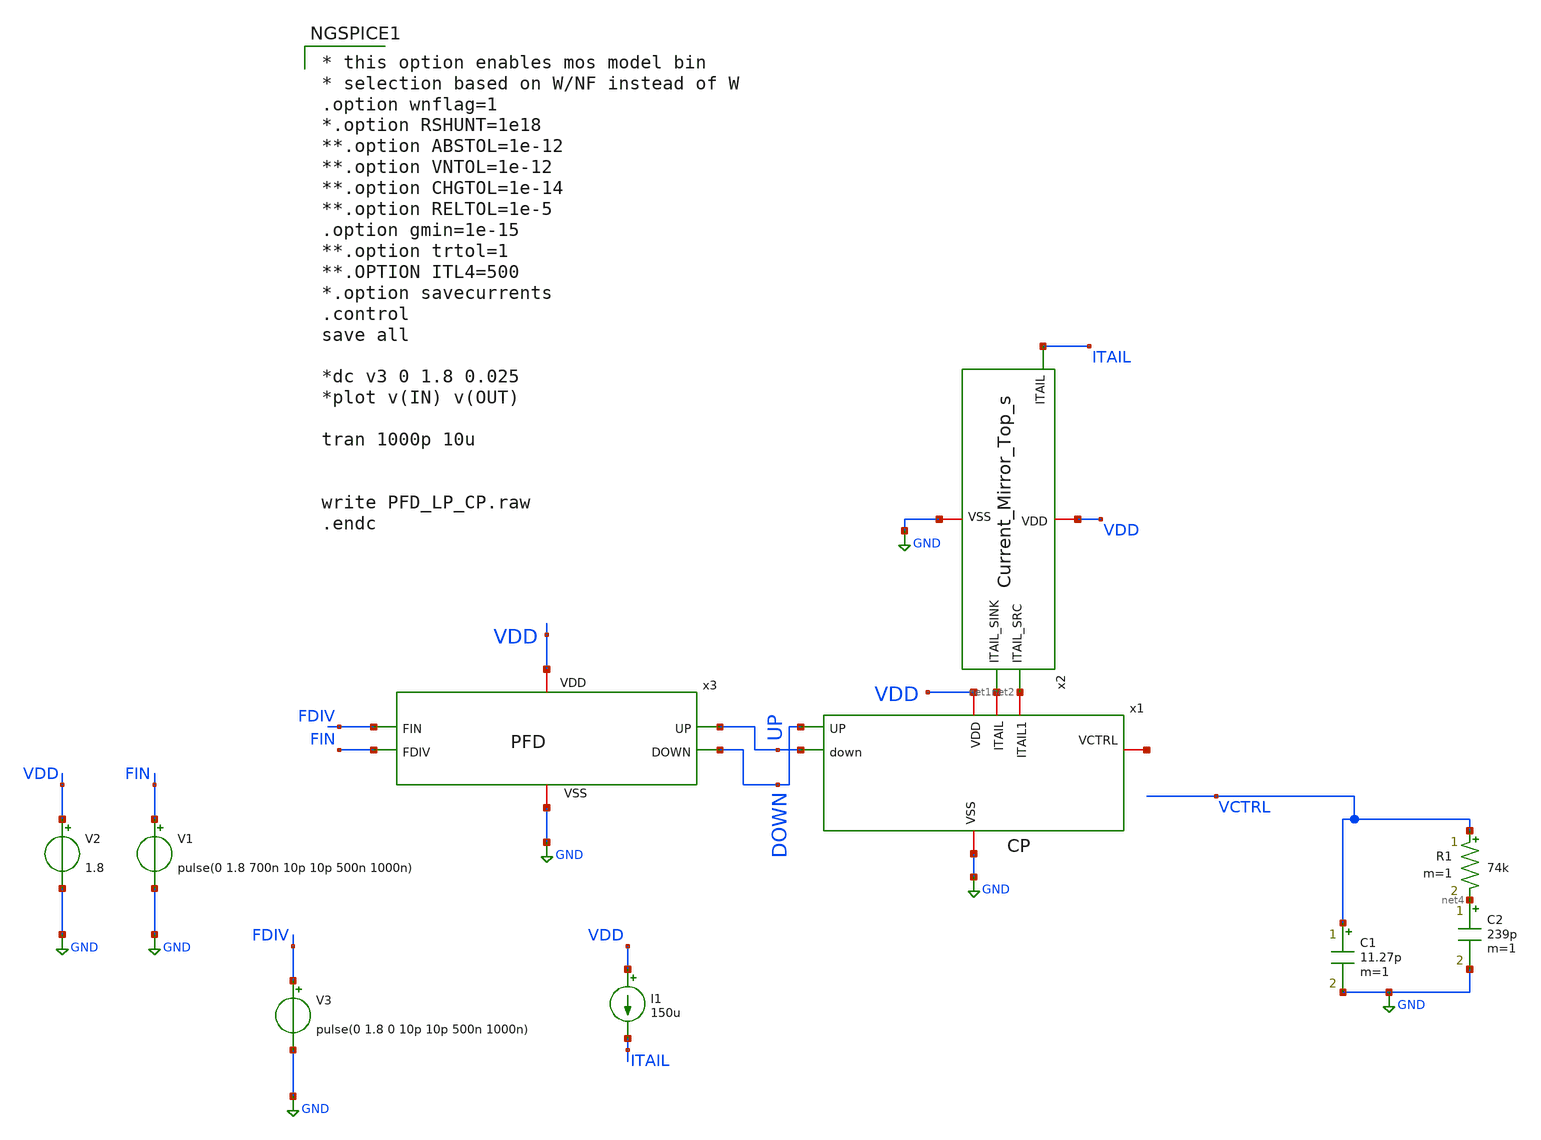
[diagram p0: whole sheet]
** sch_path: Xschem/TOP/PFD_LP_CP.sch
**.subckt PFD_LP_CP
x1 VDD net1 net2 net3 DOWN UP GND CP
x2 VDD ITAIL net2 net1 GND Current_Mirror_Top_s
x3 VDD GND FDIV FIN UP DOWN PFD
C1 VCTRL GND 11.27p m=1
R1 VCTRL net4 74k m=1
C2 net4 GND 239p m=1
V2 VDD GND 1.8
V1 FIN GND pulse(0 1.8 700n 10p 10p 500n 1000n)
V3 FDIV GND pulse(0 1.8 0 10p 10p 500n 1000n)
I1 VDD ITAIL 150u
**** begin user architecture code

** opencircuitdesign pdks install
.lib $::SKYWATER_MODELS/sky130.lib.spice tt



* this option enables mos model bin
* selection based on W/NF instead of W
.option wnflag=1
*.option RSHUNT=1e18
**.option ABSTOL=1e-12
**.option VNTOL=1e-12
**.option CHGTOL=1e-14
**.option RELTOL=1e-5
.option gmin=1e-15
**.option trtol=1
**.OPTION ITL4=500
*.option savecurrents
.control
save all

*dc v3 0 1.8 0.025
*plot v(IN) v(OUT)

tran 1000p 10u


write PFD_LP_CP.raw
.endc


**** end user architecture code
**.ends
.GLOBAL GND
.end
